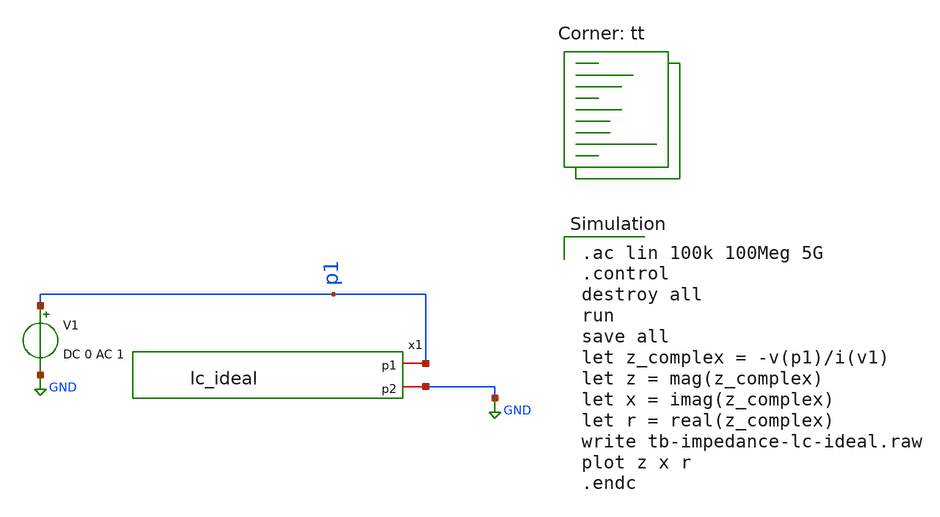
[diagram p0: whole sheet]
** sch_path: examples/sq_1nH_2.5GHz/xschem/tb-impedance-lc-ideal.sch
**.subckt tb-impedance-lc-ideal
V1 p1 GND DC 0 AC 1
x1 p1 GND lc_ideal
**** begin user architecture code

.ac lin 100k 100Meg 5G
.control
destroy all
run
save all
let z_complex = -v(p1)/i(v1)
let z = mag(z_complex)
let x = imag(z_complex)
let r = real(z_complex)
write tb-impedance-lc-ideal.raw
plot z x r
.endc

.lib $::SKYWATER_MODELS/sky130.lib.spice tt
**** end user architecture code
**.ends

* expanding   symbol:  /foss/designs/asitic-example/examples/sq_1nH_2.5GHz/xschem/lc_ideal.sym # of
*+ pins=2
** sym_path: examples/sq_1nH_2.5GHz/xschem/lc_ideal.sym
** sch_path: examples/sq_1nH_2.5GHz/xschem/lc_ideal.sch
.subckt lc_ideal p1 p2
*.iopin p1
*.iopin p2
C1 p1 p2 4.0528p m=1
L1 p1 p2 1n m=1
.ends

.GLOBAL GND
.end
